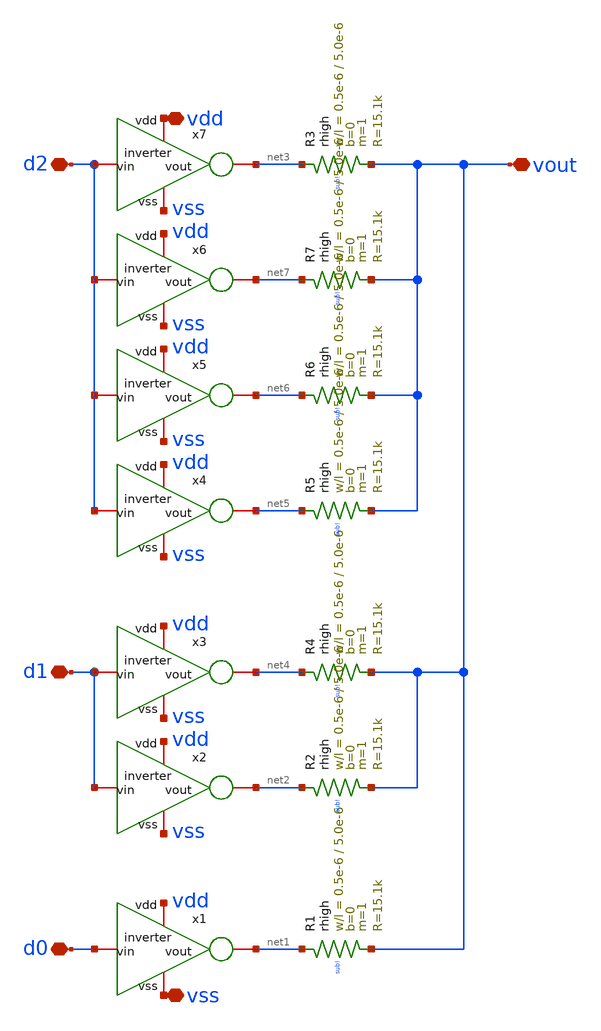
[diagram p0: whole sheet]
** sch_path: xschem/rdac_weighted.sch
**.subckt rdac_weighted vout d0 d1 vdd d2 vss
*.iopin vout
*.iopin d0
*.iopin d1
*.iopin vdd
*.iopin d2
*.iopin vss
x1 vdd d0 net1 vss inverter
XR1 net1 vout sub! rhigh w=0.5e-6 l=5.0e-6 m=1 b=0 mm_ok=1
x2 vdd d1 net2 vss inverter
XR2 net2 vout sub! rhigh w=0.5e-6 l=5.0e-6 m=1 b=0 mm_ok=1
x7 vdd d2 net3 vss inverter
XR3 net3 vout sub! rhigh w=0.5e-6 l=5.0e-6 m=1 b=0 mm_ok=1
x3 vdd d1 net4 vss inverter
XR4 net4 vout sub! rhigh w=0.5e-6 l=5.0e-6 m=1 b=0 mm_ok=1
x4 vdd d2 net5 vss inverter
XR5 net5 vout sub! rhigh w=0.5e-6 l=5.0e-6 m=1 b=0 mm_ok=1
x5 vdd d2 net6 vss inverter
XR6 net6 vout sub! rhigh w=0.5e-6 l=5.0e-6 m=1 b=0 mm_ok=1
x6 vdd d2 net7 vss inverter
XR7 net7 vout sub! rhigh w=0.5e-6 l=5.0e-6 m=1 b=0 mm_ok=1
**.ends

* expanding   symbol:  inverter.sym # of pins=4
** sym_path: xschem/inverter.sym
** sch_path: xschem/inverter.sch
.subckt inverter vdd vin vout vss
*.iopin vout
*.iopin vss
*.iopin vin
*.iopin vdd
XM1 vout vin vss vss sg13_lv_nmos w=1.5u l=0.13u ng=1 m=1 mm_ok=1
XM2 vout vin vdd vdd sg13_lv_pmos w=3.0u l=0.13u ng=1 m=1 mm_ok=1
.ends

.end
